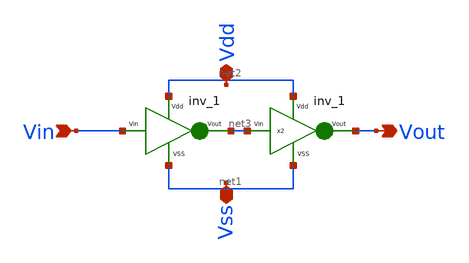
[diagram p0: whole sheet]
** sch_path: xschem files/buffer.sch
**.subckt buffer Vin Vdd Vss Vout
*.ipin Vin
*.iopin Vdd
*.iopin Vss
*.opin Vout
x1 net2 net3 Vin net1 inv_1
x2 net2 Vout net3 net1 inv_1
**.ends

* expanding   symbol:  /home/harshit/.xschem/inv_1.sym # of pins=4
** sym_path: xschem files/inv_1.sym
** sch_path: xschem files/inv_1.sch
.subckt inv_1 Vdd Vout Vin VSS
*.ipin Vdd
*.ipin VSS
*.opin Vout
*.ipin Vin
XM1 Vout Vin VSS VSS sky130_fd_pr__nfet_01v8 L=0.15 W=1.05 nf=1 ad='int((nf+1)/2) * W/nf * 0.29' as='int((nf+2)/2) * W/nf * 0.29'
+ pd='2*int((nf+1)/2) * (W/nf + 0.29)' ps='2*int((nf+2)/2) * (W/nf + 0.29)' nrd='0.29 / W' nrs='0.29 / W'
+ sa=0 sb=0 sd=0 mult=1 m=1
XM2 Vout Vin Vdd Vdd sky130_fd_pr__pfet_01v8 L=0.15 W=2.1 nf=1 ad='int((nf+1)/2) * W/nf * 0.29' as='int((nf+2)/2) * W/nf * 0.29'
+ pd='2*int((nf+1)/2) * (W/nf + 0.29)' ps='2*int((nf+2)/2) * (W/nf + 0.29)' nrd='0.29 / W' nrs='0.29 / W'
+ sa=0 sb=0 sd=0 mult=1 m=1
.ends

.end
